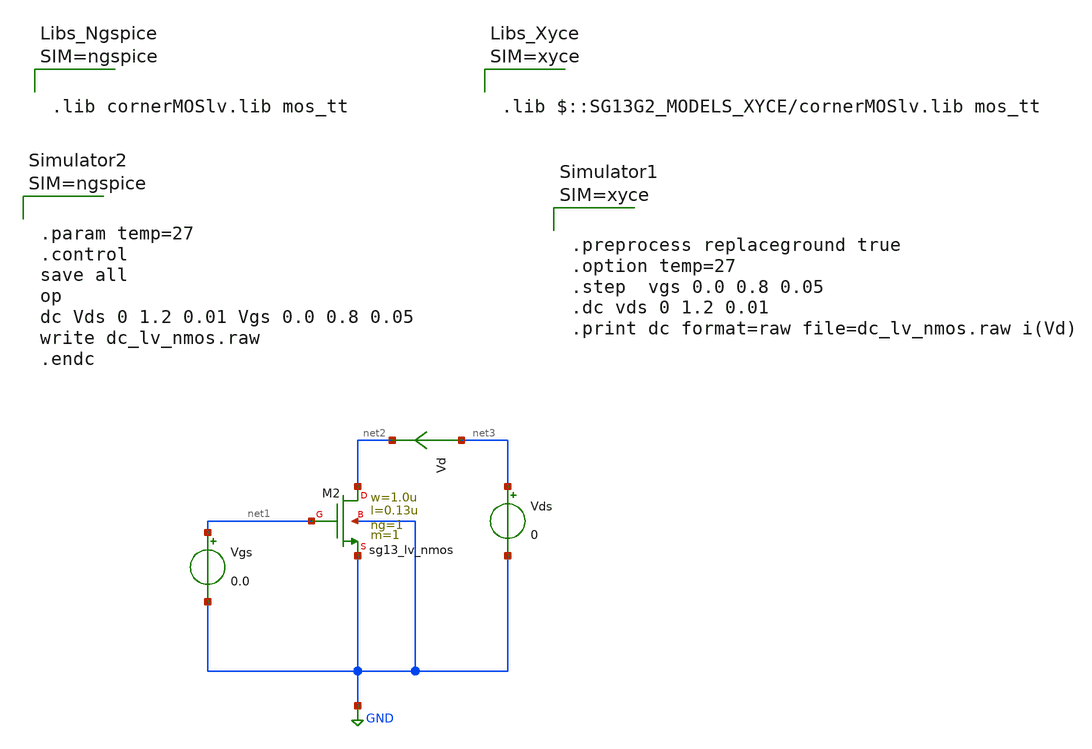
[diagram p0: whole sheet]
** sch_path: ihp-sg13g2/libs.tech/xschem/sg13g2_tests_xyce/dc_lv_nmos.sch
* Copyright 2023 IHP PDK Authors
**.subckt dc_lv_nmos
Vgs net1 GND 0.0
Vds net3 GND 0
Vd net3 net2 0
.save i(vd)
XM2 net2 net1 GND GND sg13_lv_nmos w=1.0u l=0.13u ng=1 m=1 mm_ok=1
**** begin user architecture code









.lib cornerMOSlv.lib mos_tt






.param temp=27
.control
save all
op
dc Vds 0 1.2 0.01 Vgs 0.0 0.8 0.05
write dc_lv_nmos.raw
.endc



**** end user architecture code
**.ends
.GLOBAL GND
.end
